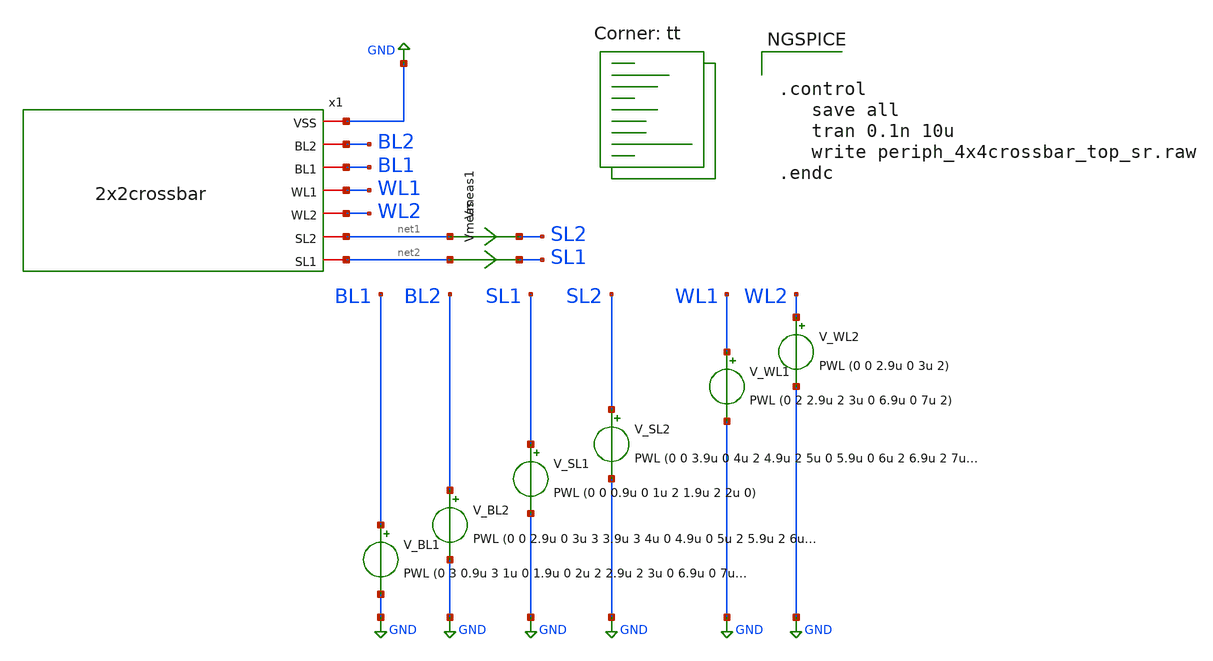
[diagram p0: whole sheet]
** sch_path: xschem/test/xschem/periph_4x4crossbar_top_sr.sch
* StefanSchippers/xschem_sky130/sky130_fd_pr/reram.sym:
* Copyright 2021 Stefan Frederik Schippers
* Licensed under the Apache License, Version 2.0 (the "License");
**.subckt periph_4x4crossbar_top_sr
V_BL1 BL1 GND PWL (0 3 0.9u 3 1u 0 1.9u 0 2u 2 2.9u 2 3u 0 6.9u 0 7u 0.2)
V_BL2 BL2 GND PWL (0 0 2.9u 0 3u 3 3.9u 3 4u 0 4.9u 0 5u 2 5.9u 2 6u 0 6.9u 0 7u 0.2)
x1 GND BL2 BL1 WL1 WL2 net1 net2 2x2crossbar
V_WL1 WL1 GND PWL (0 2 2.9u 2 3u 0 6.9u 0 7u 2)
V_WL2 WL2 GND PWL (0 0 2.9u 0 3u 2)
Vmeas1 net1 SL2 0
.save i(vmeas1)
Vmeas net2 SL1 0
.save i(vmeas)
V_SL1 SL1 GND PWL (0 0 0.9u 0 1u 2 1.9u 2 2u 0)
V_SL2 SL2 GND PWL (0 0 3.9u 0 4u 2 4.9u 2 5u 0 5.9u 0 6u 2 6.9u 2 7u 0)
**** begin user architecture code
.lib $::SKYWATER_MODELS/sky130.lib.spice tt


.control
   save all
   tran 0.1n 10u
   write periph_4x4crossbar_top_sr.raw
.endc


**** end user architecture code
**.ends

* expanding   symbol:  2x2crossbar.sym # of pins=7
** sym_path: 2x2crossbar.sym
** sch_path: 2x2crossbar.sch
.subckt 2x2crossbar VSS BL2 BL1 WL1 WL2 SL2 SL1
*.iopin BL2
*.iopin BL1
*.iopin WL1
*.iopin WL2
*.iopin SL1
*.iopin SL2
*.iopin VSS
x1 BL1 WL1 SL1 VSS 1T1R
x2 BL2 WL1 SL2 VSS 1T1R
x3 BL1 WL2 SL1 VSS 1T1R
x4 BL2 WL2 SL2 VSS 1T1R
.ends


* expanding   symbol:  1T1R.sym # of pins=4
** sym_path: xschem/test/xschem/1T1R.sym
** sch_path: xschem/test/xschem/1T1R.sch
.subckt 1T1R BL WL SL VSS
*.iopin SL
*.iopin WL
*.iopin BL
*.iopin VSS
XR1 BL net1 sky130_fd_pr_reram__reram_cell Tfilament_0=3.8e-9
XM1 net1 WL SL VSS sky130_fd_pr__nfet_g5v0d10v5 L=0.5 W=7 nf=1 ad='int((nf+1)/2) * W/nf * 0.29' as='int((nf+2)/2) * W/nf * 0.29'
+ pd='2*int((nf+1)/2) * (W/nf + 0.29)' ps='2*int((nf+2)/2) * (W/nf + 0.29)' nrd='0.29 / W' nrs='0.29 / W'
+ sa=0 sb=0 sd=0 mult=1 m=1
.ends

.GLOBAL GND
**** begin user architecture code

.subckt sky130_fd_pr_reram__reram_cell TE BE Tfilament_0=3.3e-9 area_ox=0.1024e-12
N1 TE BE nFilament sky130_fd_pr_reram__reram_model
.ic v(nFilament)={Tfilament_0*1.0e9}
.ends sky130_fd_pr_reram__reram_cell

.model sky130_fd_pr_reram__reram_model sky130_fd_pr_reram__reram_module  area_ox = 0.1024e-12  Tox =
+ 5.0  Tfilament_max = 4.9  Tfilament_min = 3.3  Eact_generation = 1.501  Eact_recombination  = 1.500
+  I_k1  = 6.140e-5  Tfilament_ref = 4.7249  V_ref = 0.430  velocity_k1 = 150  gamma_k0  = 16.5  gamma_k1
+  = -1.25  Temperature_0 = 300  C_thermal = 3.1825e-16  tau_thermal = 0.23e-9  t_step  = 1.0e-9
+  smoothing = 1e-7  Kclip = 200

.control
pre_osdi $SKYWATER_MODELS/sky130_fd_pr_reram__reram_module.osdi
.endc

**** end user architecture code
.end
